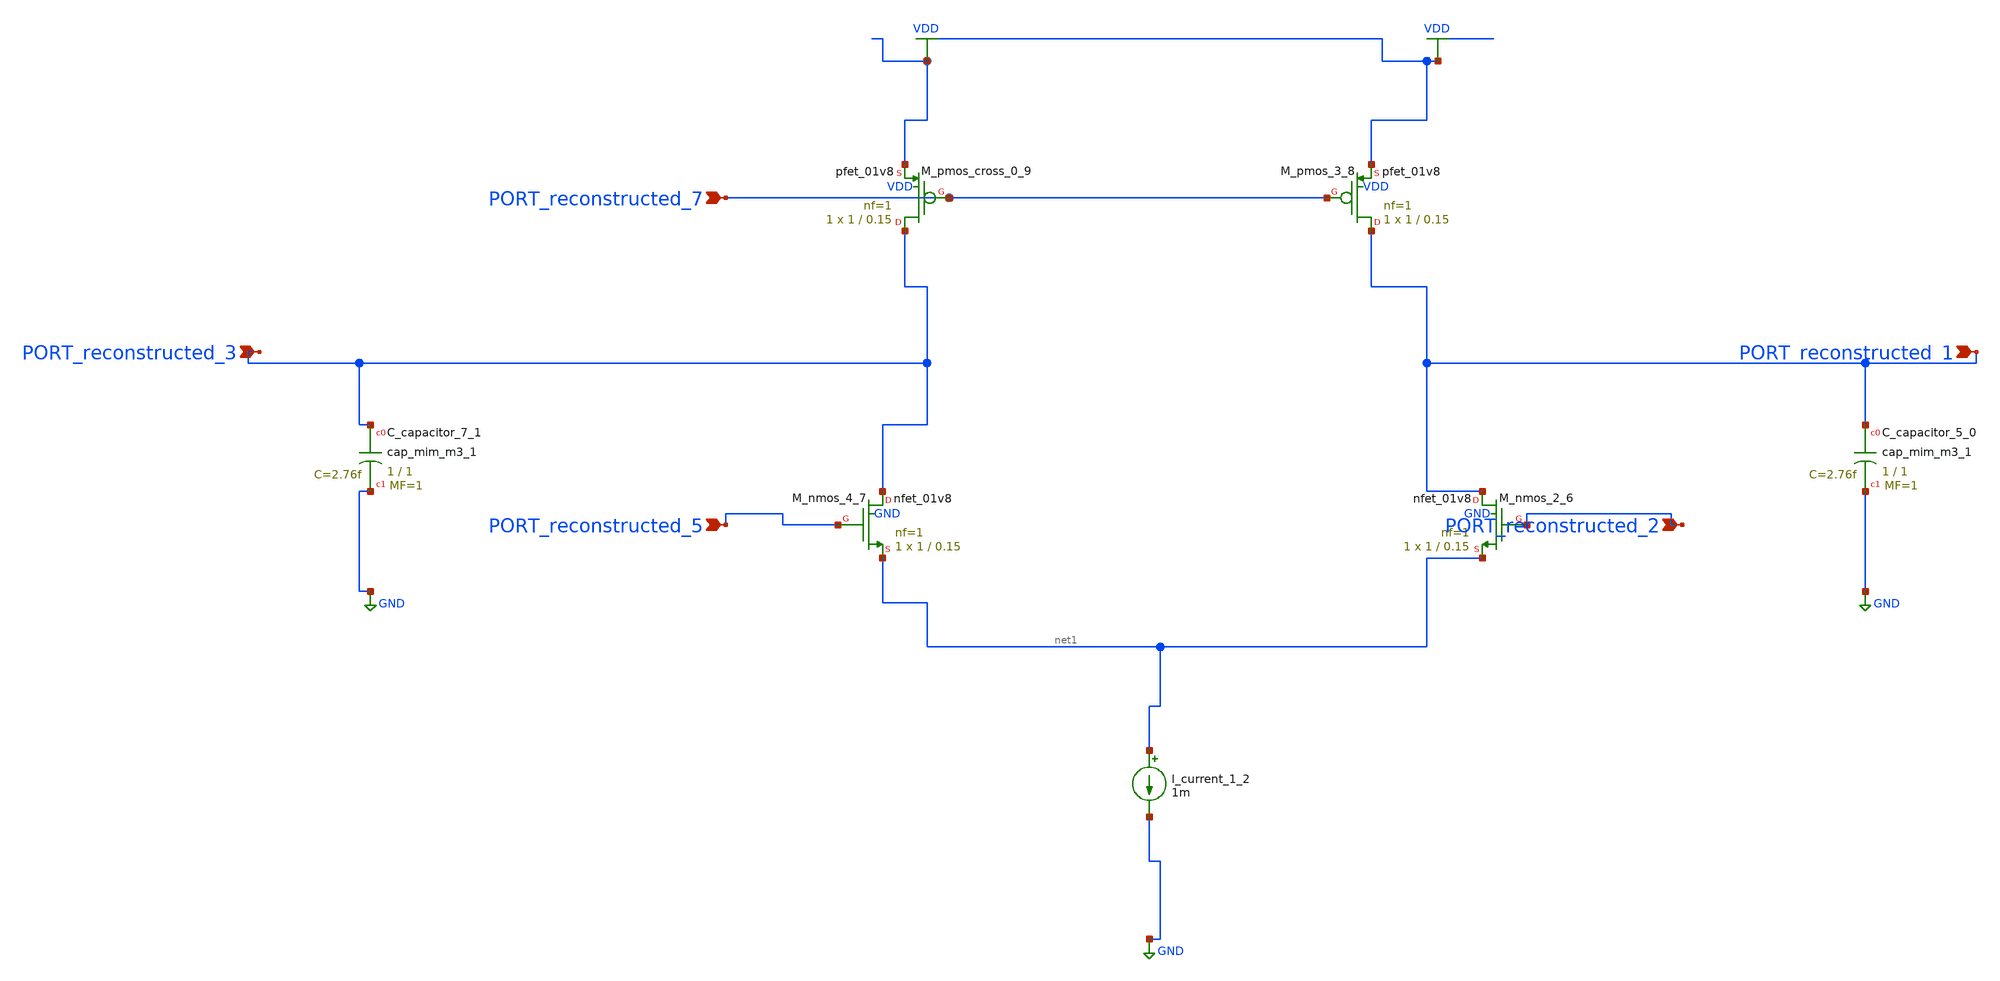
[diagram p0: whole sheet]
** sch_path: schematics/AMSNet/626.sch
**.subckt 626 PORT_reconstructed_5 PORT_reconstructed_1 PORT_reconstructed_2 PORT_reconstructed_7
*+ PORT_reconstructed_3
*.ipin PORT_reconstructed_5
*.ipin PORT_reconstructed_1
*.ipin PORT_reconstructed_2
*.ipin PORT_reconstructed_7
*.ipin PORT_reconstructed_3
XC_capacitor_5_0 PORT_reconstructed_1 GND sky130_fd_pr__cap_mim_m3_1 W=1 L=1 MF=1 m=1
XC_capacitor_7_1 PORT_reconstructed_3 GND sky130_fd_pr__cap_mim_m3_1 W=1 L=1 MF=1 m=1
I_current_1_2 net1 GND 1m
XM_nmos_2_6 PORT_reconstructed_1 PORT_reconstructed_2 net1 GND sky130_fd_pr__nfet_01v8 L=0.15 W=1 nf=1
+ ad='int((1 + 1)/2) * 1 / 1 * 0.29' as='int((1 + 2)/2) * 1 / 1 * 0.29' pd='2*int((1 + 1)/2) * (1 / 1 + 0.29)'
+ ps='2*int((1 + 2)/2) * (1 / 1 + 0.29)' nrd='0.29 / 1 ' nrs='0.29 / 1 ' sa=0 sb=0 sd=0 mult=1 m=1
XM_nmos_4_7 PORT_reconstructed_3 PORT_reconstructed_5 net1 GND sky130_fd_pr__nfet_01v8 L=0.15 W=1 nf=1
+ ad='int((1 + 1)/2) * 1 / 1 * 0.29' as='int((1 + 2)/2) * 1 / 1 * 0.29' pd='2*int((1 + 1)/2) * (1 / 1 + 0.29)'
+ ps='2*int((1 + 2)/2) * (1 / 1 + 0.29)' nrd='0.29 / 1 ' nrs='0.29 / 1 ' sa=0 sb=0 sd=0 mult=1 m=1
XM_pmos_3_8 PORT_reconstructed_1 PORT_reconstructed_7 VDD VDD sky130_fd_pr__pfet_01v8 L=0.15 W=1 nf=1
+ ad='int((1 + 1)/2) * 1 / 1 * 0.29' as='int((1 + 2)/2) * 1 / 1 * 0.29' pd='2*int((1 + 1)/2) * (1 / 1 + 0.29)'
+ ps='2*int((1 + 2)/2) * (1 / 1 + 0.29)' nrd='0.29 / 1 ' nrs='0.29 / 1 ' sa=0 sb=0 sd=0 mult=1 m=1
XM_pmos_cross_0_9 PORT_reconstructed_3 PORT_reconstructed_7 VDD VDD sky130_fd_pr__pfet_01v8 L=0.15 W=1
+ nf=1 ad='int((1 + 1)/2) * 1 / 1 * 0.29' as='int((1 + 2)/2) * 1 / 1 * 0.29' pd='2*int((1 + 1)/2) * (1 / 1 + 0.29)'
+ ps='2*int((1 + 2)/2) * (1 / 1 + 0.29)' nrd='0.29 / 1 ' nrs='0.29 / 1 ' sa=0 sb=0 sd=0 mult=1 m=1
**.ends
.GLOBAL GND
.GLOBAL VDD
.end
